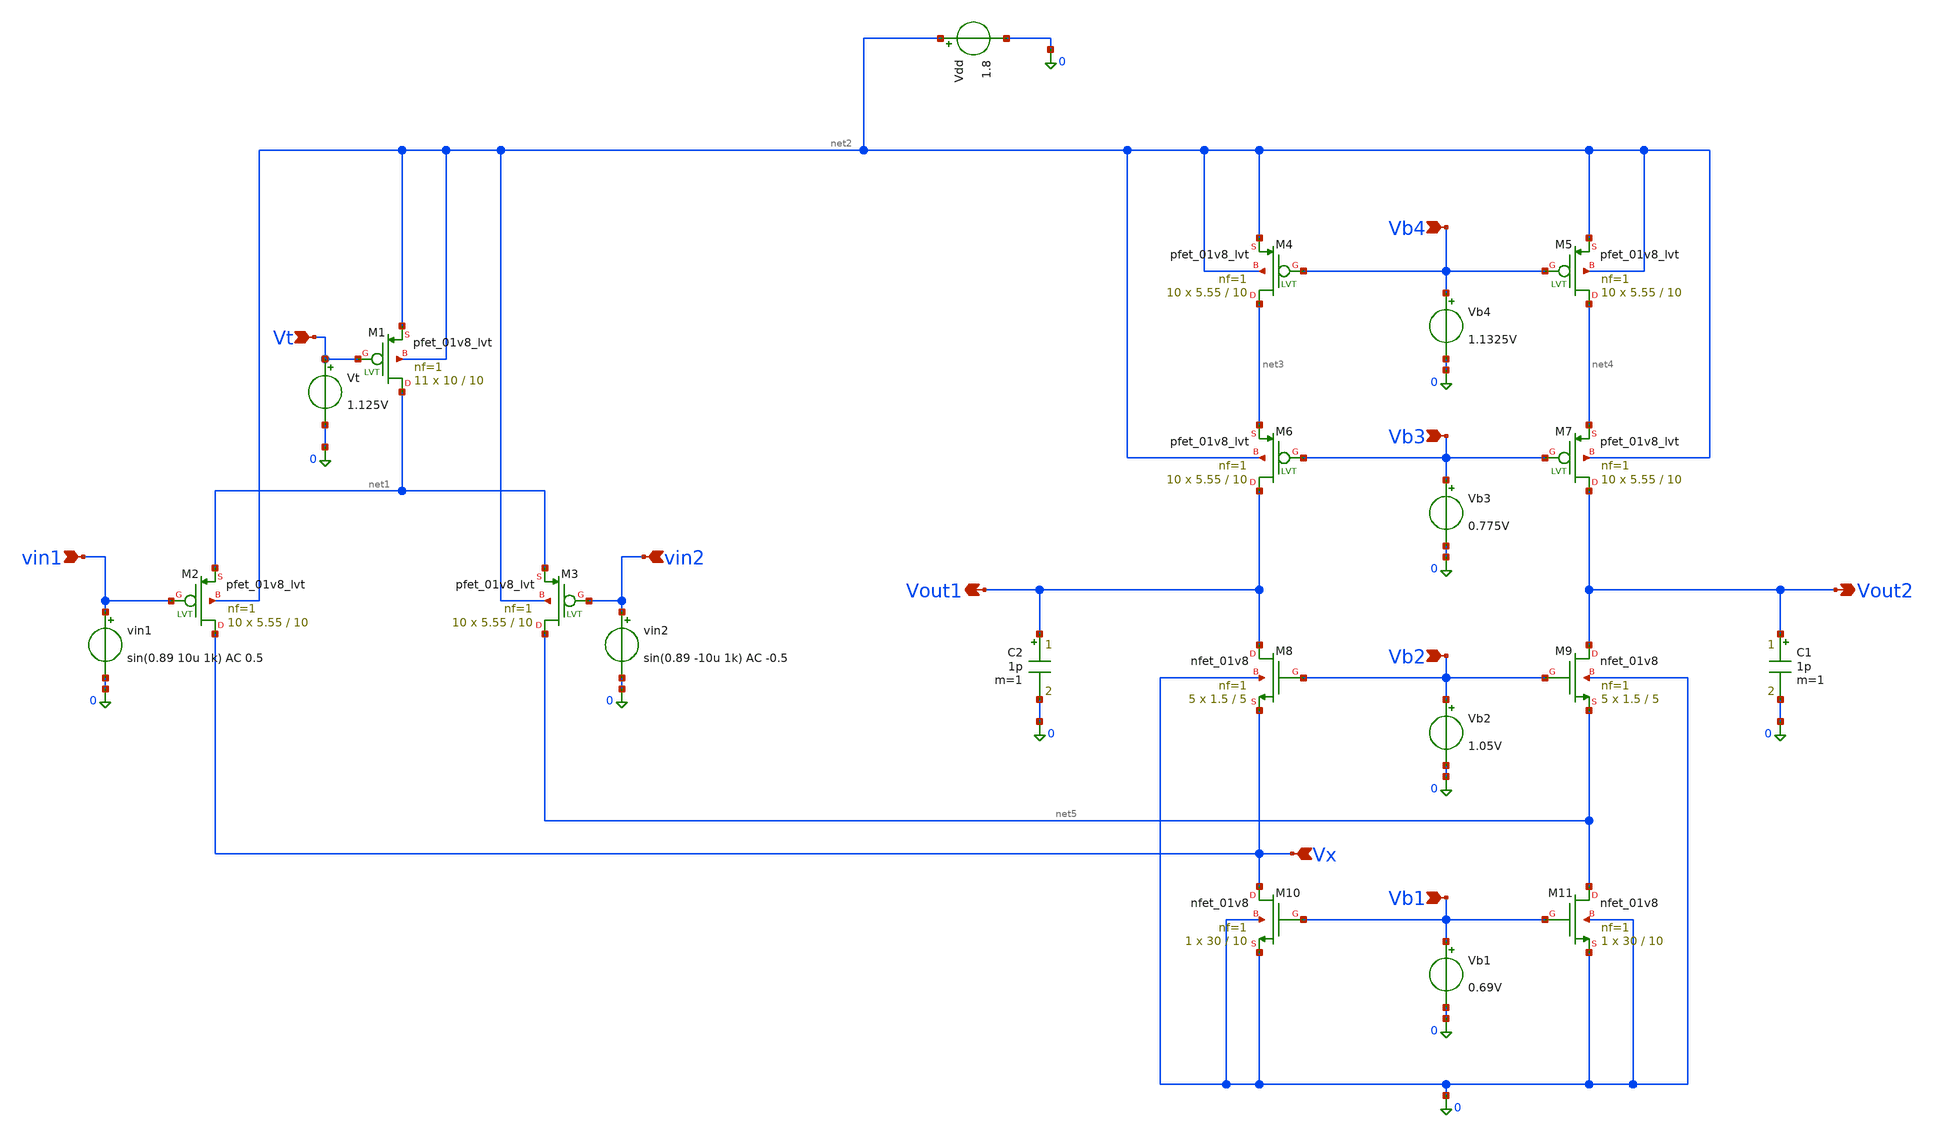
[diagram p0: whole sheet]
** sch_path: diff_folded_cascade.sch
**.subckt diff_folded_cascade Vout2 vin1 vin2 Vt Vout1 Vb4 Vb3 Vb2 Vb1 Vx
*.opin Vout2
*.ipin vin1
*.ipin vin2
*.ipin Vt
*.opin Vout1
*.ipin Vb4
*.ipin Vb3
*.ipin Vb2
*.ipin Vb1
*.ipin Vx
Vdd net2 0 1.8
C1 Vout2 0 1p m=1
XM2 Vx vin1 net1 net2 sky130_fd_pr__pfet_01v8_lvt L=10 W=5.55 nf=1 ad='int((1 + 1)/2) * 5.55 / 1 * 0.29'
+ as='int((1 + 2)/2) * 5.55 / 1 * 0.29' pd='2*int((1 + 1)/2) * (5.55 / 1 + 0.29)' ps='2*int((1 + 2)/2) * (5.55 / 1 + 0.29)'
+ nrd='0.29 / 5.55 ' nrs='0.29 / 5.55 ' sa=0 sb=0 sd=0 mult=10 m=10
XM3 net5 vin2 net1 net2 sky130_fd_pr__pfet_01v8_lvt L=10 W=5.55 nf=1 ad='int((1 + 1)/2) * 5.55 / 1 * 0.29'
+ as='int((1 + 2)/2) * 5.55 / 1 * 0.29' pd='2*int((1 + 1)/2) * (5.55 / 1 + 0.29)' ps='2*int((1 + 2)/2) * (5.55 / 1 + 0.29)'
+ nrd='0.29 / 5.55 ' nrs='0.29 / 5.55 ' sa=0 sb=0 sd=0 mult=10 m=10
vin1 vin1 0 sin(0.89 10u 1k) AC 0.5
vin2 vin2 0 sin(0.89 -10u 1k) AC -0.5
XM1 net1 Vt net2 net2 sky130_fd_pr__pfet_01v8_lvt L=10 W=10 nf=1 ad='int((1 + 1)/2) * 10 / 1 * 0.29'
+ as='int((1 + 2)/2) * 10 / 1 * 0.29' pd='2*int((1 + 1)/2) * (10 / 1 + 0.29)' ps='2*int((1 + 2)/2) * (10 / 1 + 0.29)'
+ nrd='0.29 / 10 ' nrs='0.29 / 10 ' sa=0 sb=0 sd=0 mult=11 m=11
XM4 net3 Vb4 net2 net2 sky130_fd_pr__pfet_01v8_lvt L=10 W=5.55 nf=1 ad='int((1 + 1)/2) * 5.55 / 1 * 0.29'
+ as='int((1 + 2)/2) * 5.55 / 1 * 0.29' pd='2*int((1 + 1)/2) * (5.55 / 1 + 0.29)' ps='2*int((1 + 2)/2) * (5.55 / 1 + 0.29)'
+ nrd='0.29 / 5.55 ' nrs='0.29 / 5.55 ' sa=0 sb=0 sd=0 mult=10 m=10
XM8 Vout1 Vb2 Vx 0 sky130_fd_pr__nfet_01v8 L=5 W=1.5 nf=1 ad='int((1 + 1)/2) * 1.5 / 1 * 0.29' as='int((1 + 2)/2) * 1.5 / 1 * 0.29'
+ pd='2*int((1 + 1)/2) * (1.5 / 1 + 0.29)' ps='2*int((1 + 2)/2) * (1.5 / 1 + 0.29)' nrd='0.29 / 1.5 ' nrs='0.29 / 1.5 '
+ sa=0 sb=0 sd=0 mult=5 m=5
XM9 Vout2 Vb2 net5 0 sky130_fd_pr__nfet_01v8 L=5 W=1.5 nf=1 ad='int((1 + 1)/2) * 1.5 / 1 * 0.29' as='int((1 + 2)/2) * 1.5 / 1 * 0.29'
+ pd='2*int((1 + 1)/2) * (1.5 / 1 + 0.29)' ps='2*int((1 + 2)/2) * (1.5 / 1 + 0.29)' nrd='0.29 / 1.5 ' nrs='0.29 / 1.5 '
+ sa=0 sb=0 sd=0 mult=5 m=5
XM10 Vx Vb1 0 0 sky130_fd_pr__nfet_01v8 L=10 W=30 nf=1 ad='int((1 + 1)/2) * 30 / 1 * 0.29' as='int((1 + 2)/2) * 30 / 1 * 0.29'
+ pd='2*int((1 + 1)/2) * (30 / 1 + 0.29)' ps='2*int((1 + 2)/2) * (30 / 1 + 0.29)' nrd='0.29 / 30 ' nrs='0.29 / 30 '
+ sa=0 sb=0 sd=0 mult=1 m=1
XM11 net5 Vb1 0 0 sky130_fd_pr__nfet_01v8 L=10 W=30 nf=1 ad='int((1 + 1)/2) * 30 / 1 * 0.29' as='int((1 + 2)/2) * 30 / 1 * 0.29'
+ pd='2*int((1 + 1)/2) * (30 / 1 + 0.29)' ps='2*int((1 + 2)/2) * (30 / 1 + 0.29)' nrd='0.29 / 30 ' nrs='0.29 / 30 '
+ sa=0 sb=0 sd=0 mult=1 m=1
XM5 net4 Vb4 net2 net2 sky130_fd_pr__pfet_01v8_lvt L=10 W=5.55 nf=1 ad='int((1 + 1)/2) * 5.55 / 1 * 0.29'
+ as='int((1 + 2)/2) * 5.55 / 1 * 0.29' pd='2*int((1 + 1)/2) * (5.55 / 1 + 0.29)' ps='2*int((1 + 2)/2) * (5.55 / 1 + 0.29)'
+ nrd='0.29 / 5.55 ' nrs='0.29 / 5.55 ' sa=0 sb=0 sd=0 mult=10 m=10
XM6 Vout1 Vb3 net3 net2 sky130_fd_pr__pfet_01v8_lvt L=10 W=5.55 nf=1 ad='int((1 + 1)/2) * 5.55 / 1 * 0.29'
+ as='int((1 + 2)/2) * 5.55 / 1 * 0.29' pd='2*int((1 + 1)/2) * (5.55 / 1 + 0.29)' ps='2*int((1 + 2)/2) * (5.55 / 1 + 0.29)'
+ nrd='0.29 / 5.55 ' nrs='0.29 / 5.55 ' sa=0 sb=0 sd=0 mult=10 m=10
XM7 Vout2 Vb3 net4 net2 sky130_fd_pr__pfet_01v8_lvt L=10 W=5.55 nf=1 ad='int((1 + 1)/2) * 5.55 / 1 * 0.29'
+ as='int((1 + 2)/2) * 5.55 / 1 * 0.29' pd='2*int((1 + 1)/2) * (5.55 / 1 + 0.29)' ps='2*int((1 + 2)/2) * (5.55 / 1 + 0.29)'
+ nrd='0.29 / 5.55 ' nrs='0.29 / 5.55 ' sa=0 sb=0 sd=0 mult=10 m=10
Vt Vt 0 1.125V
C2 Vout1 0 1p m=1
Vb4 Vb4 0 1.1325V
Vb3 Vb3 0 0.775V
Vb2 Vb2 0 1.05V
Vb1 Vb1 0 0.69V
**** begin user architecture code


.lib /foss/pdks/ciel/sky130/versions/b344c97eacc2aaf8e14ae7e43e2e9dc0871de2c0/sky130A/libs.tech/ngspice/sky130.lib.spice tt

.control
  option temp = 27
  alter vdd dc = 1.8
  set color0=white
  set color1=black
  set color2=red
  set color3=blue


  op
  echo --- Tail Transistor M1 ---
  print @m.xm1.msky130_fd_pr__pfet_01v8_lvt[id]
  print @m.xm1.msky130_fd_pr__pfet_01v8_lvt[vds]
  print @m.xm1.msky130_fd_pr__pfet_01v8_lvt[vdsat]
  print @m.xm1.msky130_fd_pr__pfet_01v8_lvt[vgs]
  print @m.xm1.msky130_fd_pr__pfet_01v8_lvt[vth]
  print @m.xm1.msky130_fd_pr__pfet_01v8_lvt[gm]
  print @m.xm1.msky130_fd_pr__pfet_01v8_lvt[gds]

  echo --- Differential Pair M2 ---
  print @m.xm2.msky130_fd_pr__pfet_01v8_lvt[id]
  print @m.xm2.msky130_fd_pr__pfet_01v8_lvt[vds]
  print @m.xm2.msky130_fd_pr__pfet_01v8_lvt[vdsat]
  print @m.xm2.msky130_fd_pr__pfet_01v8_lvt[vgs]
  print @m.xm2.msky130_fd_pr__pfet_01v8_lvt[vth]
  print @m.xm2.msky130_fd_pr__pfet_01v8_lvt[gm]
  print @m.xm2.msky130_fd_pr__pfet_01v8_lvt[gds]

  echo --- Differential Pair M3 ---
  print @m.xm3.msky130_fd_pr__pfet_01v8_lvt[id]
  print @m.xm3.msky130_fd_pr__pfet_01v8_lvt[vds]
  print @m.xm3.msky130_fd_pr__pfet_01v8_lvt[vdsat]
  print @m.xm3.msky130_fd_pr__pfet_01v8_lvt[vgs]
  print @m.xm3.msky130_fd_pr__pfet_01v8_lvt[vth]
  print @m.xm3.msky130_fd_pr__pfet_01v8_lvt[gm]
  print @m.xm3.msky130_fd_pr__pfet_01v8_lvt[gds]

  echo --- Top cascade M4 ---
  print @m.xm4.msky130_fd_pr__pfet_01v8_lvt[id]
  print @m.xm4.msky130_fd_pr__pfet_01v8_lvt[vds]
  print @m.xm4.msky130_fd_pr__pfet_01v8_lvt[vdsat]
  print @m.xm4.msky130_fd_pr__pfet_01v8_lvt[vgs]
  print @m.xm4.msky130_fd_pr__pfet_01v8_lvt[vth]
  print @m.xm4.msky130_fd_pr__pfet_01v8_lvt[gm]
  print @m.xm4.msky130_fd_pr__pfet_01v8_lvt[gds]

  echo --- Top cascade M5 ---
  print @m.xm5.msky130_fd_pr__pfet_01v8_lvt[id]
  print @m.xm5.msky130_fd_pr__pfet_01v8_lvt[vds]
  print @m.xm5.msky130_fd_pr__pfet_01v8_lvt[vdsat]
  print @m.xm5.msky130_fd_pr__pfet_01v8_lvt[vgs]
  print @m.xm5.msky130_fd_pr__pfet_01v8_lvt[vth]
  print @m.xm5.msky130_fd_pr__pfet_01v8_lvt[gm]
  print @m.xm5.msky130_fd_pr__pfet_01v8_lvt[gds]

  echo --- Cascode M6 ---
  print @m.xm6.msky130_fd_pr__pfet_01v8_lvt[id]
  print @m.xm6.msky130_fd_pr__pfet_01v8_lvt[vds]
  print @m.xm6.msky130_fd_pr__pfet_01v8_lvt[vdsat]
  print @m.xm6.msky130_fd_pr__pfet_01v8_lvt[vgs]
  print @m.xm6.msky130_fd_pr__pfet_01v8_lvt[vth]
  print @m.xm6.msky130_fd_pr__pfet_01v8_lvt[gm]
  print @m.xm6.msky130_fd_pr__pfet_01v8_lvt[gds]

  echo --- Cascode M7 ---
  print @m.xm7.msky130_fd_pr__pfet_01v8_lvt[id]
  print @m.xm7.msky130_fd_pr__pfet_01v8_lvt[vds]
  print @m.xm7.msky130_fd_pr__pfet_01v8_lvt[vdsat]
  print @m.xm7.msky130_fd_pr__pfet_01v8_lvt[vgs]
  print @m.xm7.msky130_fd_pr__pfet_01v8_lvt[vth]
  print @m.xm7.msky130_fd_pr__pfet_01v8_lvt[gm]
  print @m.xm7.msky130_fd_pr__pfet_01v8_lvt[gds]

  echo --- Bottom cascade M8 ---
  print @m.xm8.msky130_fd_pr__nfet_01v8[id]
  print @m.xm8.msky130_fd_pr__nfet_01v8[vds]
  print @m.xm8.msky130_fd_pr__nfet_01v8[vdsat]
  print @m.xm8.msky130_fd_pr__nfet_01v8[vgs]
  print @m.xm8.msky130_fd_pr__nfet_01v8[vth]
  print @m.xm8.msky130_fd_pr__nfet_01v8[gm]
  print @m.xm8.msky130_fd_pr__nfet_01v8[gds]

  echo --- Bottom cascade M9 ---
  print @m.xm9.msky130_fd_pr__nfet_01v8[id]
  print @m.xm9.msky130_fd_pr__nfet_01v8[vds]
  print @m.xm9.msky130_fd_pr__nfet_01v8[vdsat]
  print @m.xm9.msky130_fd_pr__nfet_01v8[vgs]
  print @m.xm9.msky130_fd_pr__nfet_01v8[vth]
  print @m.xm9.msky130_fd_pr__nfet_01v8[gm]
  print @m.xm9.msky130_fd_pr__nfet_01v8[gds]

  echo --- Cascade M10 ---
  print @m.xm10.msky130_fd_pr__nfet_01v8[id]
  print @m.xm10.msky130_fd_pr__nfet_01v8[vds]
  print @m.xm10.msky130_fd_pr__nfet_01v8[vdsat]
  print @m.xm10.msky130_fd_pr__nfet_01v8[vgs]
  print @m.xm10.msky130_fd_pr__nfet_01v8[vth]
  print @m.xm10.msky130_fd_pr__nfet_01v8[gm]
  print @m.xm10.msky130_fd_pr__nfet_01v8[gds]

  echo --- Cascade M11 ---
  print @m.xm11.msky130_fd_pr__nfet_01v8[id]
  print @m.xm11.msky130_fd_pr__nfet_01v8[vds]
  print @m.xm11.msky130_fd_pr__nfet_01v8[vdsat]
  print @m.xm11.msky130_fd_pr__nfet_01v8[vgs]
  print @m.xm11.msky130_fd_pr__nfet_01v8[vth]
  print @m.xm11.msky130_fd_pr__nfet_01v8[gm]
  print @m.xm11.msky130_fd_pr__nfet_01v8[gds]


* ---------- Power dissipation (DC operating point) ----------

  let i_vdd = -i(vdd)
  let p_diss = 1.8 * i_vdd

  echo --- * Supply current and Power dissipation * ---
  print i_vdd p_diss


* ---------- Differential gain: vin1 = +0.5, vin2 = -0.5 (Vid = 1 V) ----------
  ac dec 20 1 10g

* ---------- Common-mode gain: vin1 = vin2 = 1 V AC (Vic = 1 V) ----------
  alter vin1 acmag = 1
  alter vin2 acmag = 1
  ac dec 20 1 10g

* ---------- Gains and CMRR ----------
  let Ad      = ac1.vout1 - ac1.vout2
  let Acm     = (ac2.vout1 + ac2.vout2)/2
  let Ad_dB   = db(Ad)
  let Acm_dB  = db(Acm)
  let CMRR_dB = Ad_dB - Acm_dB

  echo --- Gains at 1 Hz (dB) ---
  print Ad_dB[0] Acm_dB[0] CMRR_dB[0]

  plot Ad_dB Acm_dB CMRR_dB xlog title 'Ad, Acm and CMRR (dB)'


* ---------- Transient ----------

  tran 1u 5m
  plot v(vin1) v(vin2) title 'Input: differential sine (1 kHz)'
  plot v(vout1) v(vout2) title 'Output'


* ---------- DC transfer ----------
  dc vin2 0 1.8 0.01
  plot vout1 vout2 title 'DC transfer Characteristic'


 write diff_folded_cascade.raw

.endc


**** end user architecture code
**.ends
.end
